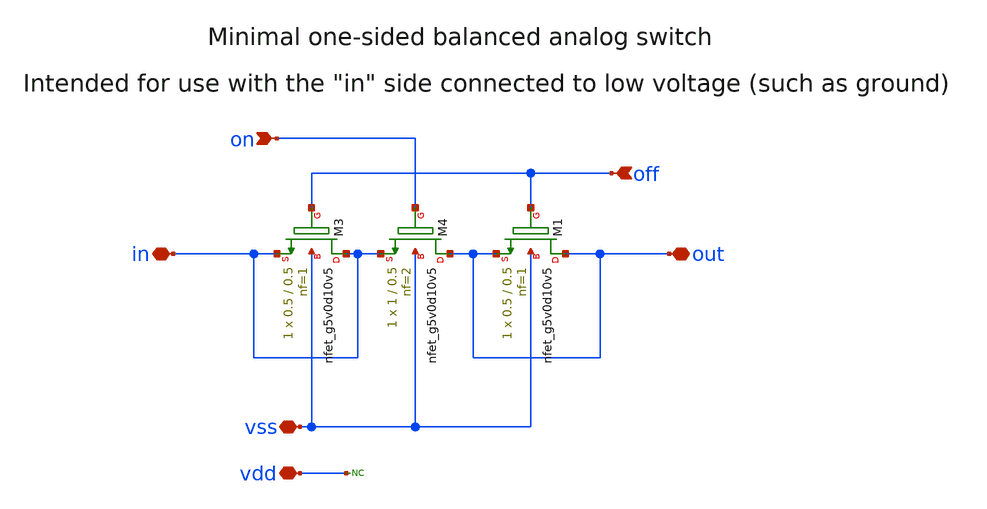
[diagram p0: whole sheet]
** sch_path: analog/repairs/adc_repaired/ip/sky130_ef_ip__cdac3v_12bit/dependencies/sky130_ef_ip__analog_switches/xschem/minimum_analog_switch.sch
**.subckt minimum_analog_switch on out vss in off vdd
*.ipin on
*.iopin out
*.iopin vss
*.iopin in
*.ipin off
*.iopin vdd
XM3 in off in vss sky130_fd_pr__nfet_g5v0d10v5 L=0.5 W=0.5 nf=1 ad='int((nf+1)/2) * W/nf * 0.29' as='int((nf+2)/2) * W/nf * 0.29'
+ pd='2*int((nf+1)/2) * (W/nf + 0.29)' ps='2*int((nf+2)/2) * (W/nf + 0.29)' nrd='0.29 / W' nrs='0.29 / W'
+ sa=0 sb=0 sd=0 mult=1 m=1
XM1 out off out vss sky130_fd_pr__nfet_g5v0d10v5 L=0.5 W=0.5 nf=1 ad='int((nf+1)/2) * W/nf * 0.29' as='int((nf+2)/2) * W/nf * 0.29'
+ pd='2*int((nf+1)/2) * (W/nf + 0.29)' ps='2*int((nf+2)/2) * (W/nf + 0.29)' nrd='0.29 / W' nrs='0.29 / W'
+ sa=0 sb=0 sd=0 mult=1 m=1
XM4 out on in vss sky130_fd_pr__nfet_g5v0d10v5 L=0.5 W=1 nf=2 ad='int((nf+1)/2) * W/nf * 0.29' as='int((nf+2)/2) * W/nf * 0.29'
+ pd='2*int((nf+1)/2) * (W/nf + 0.29)' ps='2*int((nf+2)/2) * (W/nf + 0.29)' nrd='0.29 / W' nrs='0.29 / W'
+ sa=0 sb=0 sd=0 mult=1 m=1
* noconn vdd
**.ends
.end
